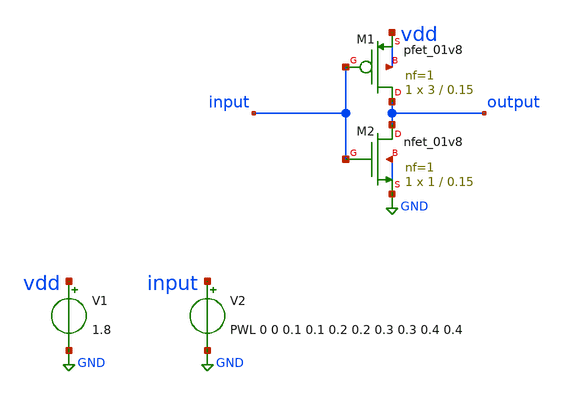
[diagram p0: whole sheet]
** sch_path: xschem/inverter_file_tb.sch
**.subckt inverter_file_tb
V1 vdd GND 1.8
XM1 output input vdd vdd sky130_fd_pr__pfet_01v8 L=0.15 W=3 nf=1 ad='int((nf+1)/2) * W/nf * 0.29' as='int((nf+2)/2) * W/nf * 0.29'
+ pd='2*int((nf+1)/2) * (W/nf + 0.29)' ps='2*int((nf+2)/2) * (W/nf + 0.29)' nrd='0.29 / W' nrs='0.29 / W'
+ sa=0 sb=0 sd=0 mult=1 m=1
XM2 output input GND GND sky130_fd_pr__nfet_01v8 L=0.15 W=1 nf=1 ad='int((nf+1)/2) * W/nf * 0.29' as='int((nf+2)/2) * W/nf * 0.29'
+ pd='2*int((nf+1)/2) * (W/nf + 0.29)' ps='2*int((nf+2)/2) * (W/nf + 0.29)' nrd='0.29 / W' nrs='0.29 / W'
+ sa=0 sb=0 sd=0 mult=1 m=1
V2 input GND PWL 0 0 0.1 0.1 0.2 0.2 0.3 0.3 0.4 0.4
**** begin user architecture code

** opencircuitdesign pdks install
.lib $::SKYWATER_MODELS/sky130.lib.spice tt





.tran 0.01 1.0
.save all

.control
run
write inverter_file_tran.raw
.endc


**** end user architecture code
**.ends
.GLOBAL GND
.end
